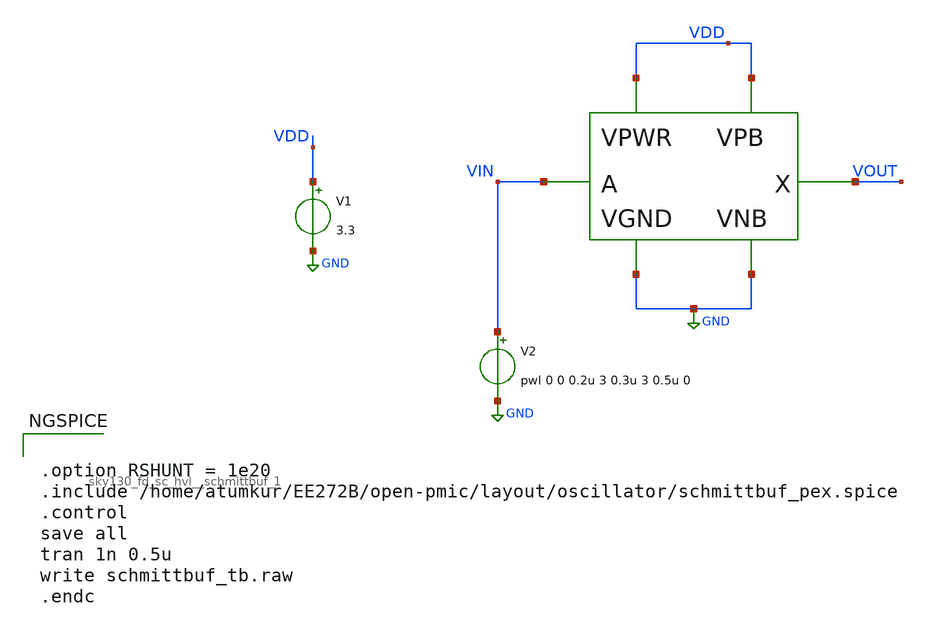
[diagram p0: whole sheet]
** sch_path: images/foss-asic-tools/addons/examples/open-pmic/layout/oscillator/schmittbuf_tb.sch
**.subckt schmittbuf_tb
V1 VDD GND 3.3
V2 VIN GND pwl 0 0 0.2u 3 0.3u 3 0.5u 0
x1 VIN GND GND VDD VDD VOUT sky130_fd_sc_hvl__schmittbuf_1
**** begin user architecture code

.include $::SKYWATER_MODELS/cells/nfet_01v8/sky130_fd_pr__nfet_01v8__tt.corner.spice
.include $::SKYWATER_MODELS/cells/nfet_01v8_lvt/sky130_fd_pr__nfet_01v8_lvt__tt.corner.spice
.include $::SKYWATER_MODELS/cells/pfet_01v8/sky130_fd_pr__pfet_01v8__tt.corner.spice
.include $::SKYWATER_MODELS/cells/nfet_03v3_nvt/sky130_fd_pr__nfet_03v3_nvt__tt.corner.spice
.include $::SKYWATER_MODELS/cells/nfet_05v0_nvt/sky130_fd_pr__nfet_05v0_nvt__tt.corner.spice
.include $::SKYWATER_MODELS/cells/esd_nfet_01v8/sky130_fd_pr__esd_nfet_01v8__tt.corner.spice
.include $::SKYWATER_MODELS/cells/pfet_01v8_lvt/sky130_fd_pr__pfet_01v8_lvt__tt.corner.spice
.include $::SKYWATER_MODELS/cells/pfet_01v8_hvt/sky130_fd_pr__pfet_01v8_hvt__tt.corner.spice
.include $::SKYWATER_MODELS/cells/esd_pfet_g5v0d10v5/sky130_fd_pr__esd_pfet_g5v0d10v5__tt.corner.spice
.include $::SKYWATER_MODELS/cells/pfet_g5v0d10v5/sky130_fd_pr__pfet_g5v0d10v5__tt.corner.spice
.include $::SKYWATER_MODELS/cells/pfet_g5v0d16v0/sky130_fd_pr__pfet_g5v0d16v0__tt.corner.spice
.include $::SKYWATER_MODELS/cells/nfet_g5v0d10v5/sky130_fd_pr__nfet_g5v0d10v5__tt.corner.spice
.include $::SKYWATER_MODELS/cells/nfet_g5v0d16v0/sky130_fd_pr__nfet_g5v0d16v0__tt_discrete.corner.spice
.include $::SKYWATER_MODELS/cells/esd_nfet_g5v0d10v5/sky130_fd_pr__esd_nfet_g5v0d10v5__tt.corner.spice
.include $::SKYWATER_MODELS/models/corners/tt/nonfet.spice
* Mismatch parameters
.include $::SKYWATER_MODELS/cells/nfet_01v8/sky130_fd_pr__nfet_01v8__mismatch.corner.spice
.include $::SKYWATER_MODELS/cells/pfet_01v8/sky130_fd_pr__pfet_01v8__mismatch.corner.spice
.include $::SKYWATER_MODELS/cells/nfet_01v8_lvt/sky130_fd_pr__nfet_01v8_lvt__mismatch.corner.spice
.include $::SKYWATER_MODELS/cells/pfet_01v8_lvt/sky130_fd_pr__pfet_01v8_lvt__mismatch.corner.spice
.include $::SKYWATER_MODELS/cells/pfet_01v8_hvt/sky130_fd_pr__pfet_01v8_hvt__mismatch.corner.spice
.include $::SKYWATER_MODELS/cells/nfet_g5v0d10v5/sky130_fd_pr__nfet_g5v0d10v5__mismatch.corner.spice
.include $::SKYWATER_MODELS/cells/pfet_g5v0d10v5/sky130_fd_pr__pfet_g5v0d10v5__mismatch.corner.spice
.include $::SKYWATER_MODELS/cells/nfet_05v0_nvt/sky130_fd_pr__nfet_05v0_nvt__mismatch.corner.spice
.include $::SKYWATER_MODELS/cells/nfet_03v3_nvt/sky130_fd_pr__nfet_03v3_nvt__mismatch.corner.spice
* Resistor$::SKYWATER_MODELS/Capacitor
.include $::SKYWATER_MODELS/models/r+c/res_typical__cap_typical.spice
.include $::SKYWATER_MODELS/models/r+c/res_typical__cap_typical__lin.spice
* Special cells
.include $::SKYWATER_MODELS/models/corners/tt/specialized_cells.spice
* All models
.include $::SKYWATER_MODELS/models/all.spice
* Corner
.include $::SKYWATER_MODELS/models/corners/tt/rf.spice



.option RSHUNT = 1e20
.include /home/atumkur/EE272B/open-pmic/layout/oscillator/schmittbuf_pex.spice
.control
save all
tran 1n 0.5u
write schmittbuf_tb.raw
.endc


**** end user architecture code
**.ends
.GLOBAL GND
**** begin user architecture code
[sky130_models]
**** end user architecture code
.end
